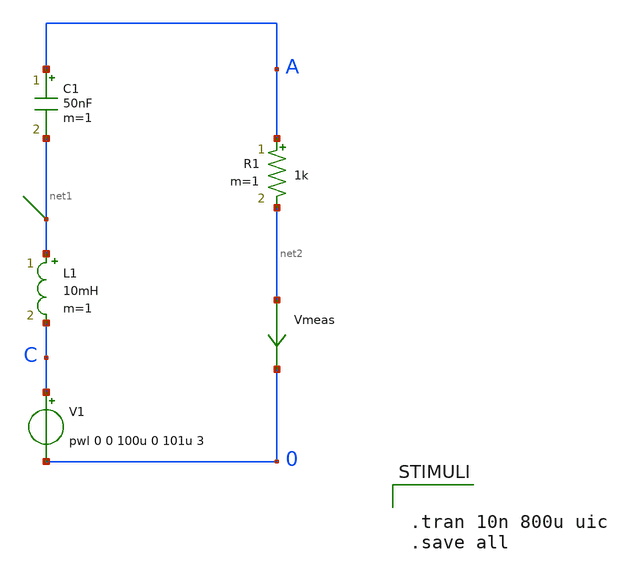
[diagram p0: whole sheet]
** sch_path: xschem_library/examples/rlc.sch
**.subckt rlc
C1 A net1 50nF m=1
R1 A net2 1k m=1
L1 net1 C 10mH m=1
V1 C 0 pwl 0 0 100u 0 101u 3
Vmeas net2 0 0
.save i(vmeas)
**** begin user architecture code


.tran 10n 800u uic
.save all


**** end user architecture code
**.ends
.end
